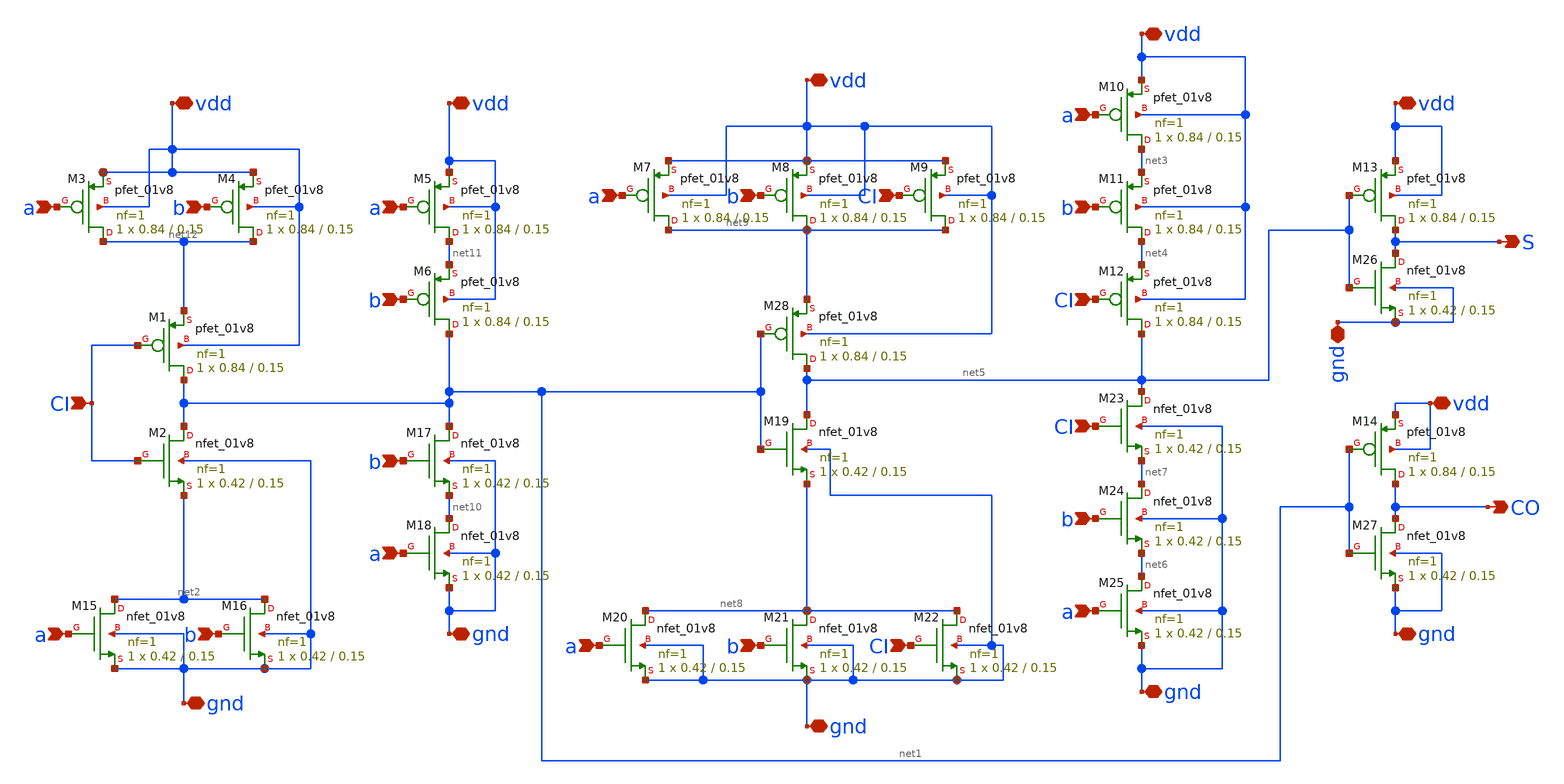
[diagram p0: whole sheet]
** sch_path: Adder/xschem/addf.sch
**.subckt addf CI CO S a a a a a a a a b b b b b b b b CI CI CI CI vdd gnd vdd vdd vdd vdd vdd gnd
*+ gnd gnd gnd gnd
*.ipin CI
*.opin CO
*.opin S
*.ipin a
*.ipin a
*.ipin a
*.ipin a
*.ipin a
*.ipin a
*.ipin a
*.ipin a
*.ipin b
*.ipin b
*.ipin b
*.ipin b
*.ipin b
*.ipin b
*.ipin b
*.ipin b
*.ipin CI
*.ipin CI
*.ipin CI
*.ipin CI
*.iopin vdd
*.iopin gnd
*.iopin vdd
*.iopin vdd
*.iopin vdd
*.iopin vdd
*.iopin vdd
*.iopin gnd
*.iopin gnd
*.iopin gnd
*.iopin gnd
*.iopin gnd
XM1 net1 CI net12 vdd sky130_fd_pr__pfet_01v8 L=0.15 W=0.84 nf=1 ad='int((nf+1)/2) * W/nf * 0.29' as='int((nf+2)/2) * W/nf * 0.29'
+ pd='2*int((nf+1)/2) * (W/nf + 0.29)' ps='2*int((nf+2)/2) * (W/nf + 0.29)' nrd='0.29 / W' nrs='0.29 / W'
+ sa=0 sb=0 sd=0 mult=1 m=1
XM2 net1 CI net2 gnd sky130_fd_pr__nfet_01v8 L=0.15 W=0.42 nf=1 ad='int((nf+1)/2) * W/nf * 0.29' as='int((nf+2)/2) * W/nf * 0.29'
+ pd='2*int((nf+1)/2) * (W/nf + 0.29)' ps='2*int((nf+2)/2) * (W/nf + 0.29)' nrd='0.29 / W' nrs='0.29 / W'
+ sa=0 sb=0 sd=0 mult=1 m=1
XM3 net12 a vdd vdd sky130_fd_pr__pfet_01v8 L=0.15 W=0.84 nf=1 ad='int((nf+1)/2) * W/nf * 0.29' as='int((nf+2)/2) * W/nf * 0.29'
+ pd='2*int((nf+1)/2) * (W/nf + 0.29)' ps='2*int((nf+2)/2) * (W/nf + 0.29)' nrd='0.29 / W' nrs='0.29 / W'
+ sa=0 sb=0 sd=0 mult=1 m=1
XM4 net12 b vdd vdd sky130_fd_pr__pfet_01v8 L=0.15 W=0.84 nf=1 ad='int((nf+1)/2) * W/nf * 0.29' as='int((nf+2)/2) * W/nf * 0.29'
+ pd='2*int((nf+1)/2) * (W/nf + 0.29)' ps='2*int((nf+2)/2) * (W/nf + 0.29)' nrd='0.29 / W' nrs='0.29 / W'
+ sa=0 sb=0 sd=0 mult=1 m=1
XM5 net11 a vdd vdd sky130_fd_pr__pfet_01v8 L=0.15 W=0.84 nf=1 ad='int((nf+1)/2) * W/nf * 0.29' as='int((nf+2)/2) * W/nf * 0.29'
+ pd='2*int((nf+1)/2) * (W/nf + 0.29)' ps='2*int((nf+2)/2) * (W/nf + 0.29)' nrd='0.29 / W' nrs='0.29 / W'
+ sa=0 sb=0 sd=0 mult=1 m=1
XM6 net1 b net11 vdd sky130_fd_pr__pfet_01v8 L=0.15 W=0.84 nf=1 ad='int((nf+1)/2) * W/nf * 0.29' as='int((nf+2)/2) * W/nf * 0.29'
+ pd='2*int((nf+1)/2) * (W/nf + 0.29)' ps='2*int((nf+2)/2) * (W/nf + 0.29)' nrd='0.29 / W' nrs='0.29 / W'
+ sa=0 sb=0 sd=0 mult=1 m=1
XM7 net9 a vdd vdd sky130_fd_pr__pfet_01v8 L=0.15 W=0.84 nf=1 ad='int((nf+1)/2) * W/nf * 0.29' as='int((nf+2)/2) * W/nf * 0.29'
+ pd='2*int((nf+1)/2) * (W/nf + 0.29)' ps='2*int((nf+2)/2) * (W/nf + 0.29)' nrd='0.29 / W' nrs='0.29 / W'
+ sa=0 sb=0 sd=0 mult=1 m=1
XM8 net9 b vdd vdd sky130_fd_pr__pfet_01v8 L=0.15 W=0.84 nf=1 ad='int((nf+1)/2) * W/nf * 0.29' as='int((nf+2)/2) * W/nf * 0.29'
+ pd='2*int((nf+1)/2) * (W/nf + 0.29)' ps='2*int((nf+2)/2) * (W/nf + 0.29)' nrd='0.29 / W' nrs='0.29 / W'
+ sa=0 sb=0 sd=0 mult=1 m=1
XM9 net9 CI vdd vdd sky130_fd_pr__pfet_01v8 L=0.15 W=0.84 nf=1 ad='int((nf+1)/2) * W/nf * 0.29' as='int((nf+2)/2) * W/nf * 0.29'
+ pd='2*int((nf+1)/2) * (W/nf + 0.29)' ps='2*int((nf+2)/2) * (W/nf + 0.29)' nrd='0.29 / W' nrs='0.29 / W'
+ sa=0 sb=0 sd=0 mult=1 m=1
XM10 net3 a vdd vdd sky130_fd_pr__pfet_01v8 L=0.15 W=0.84 nf=1 ad='int((nf+1)/2) * W/nf * 0.29' as='int((nf+2)/2) * W/nf * 0.29'
+ pd='2*int((nf+1)/2) * (W/nf + 0.29)' ps='2*int((nf+2)/2) * (W/nf + 0.29)' nrd='0.29 / W' nrs='0.29 / W'
+ sa=0 sb=0 sd=0 mult=1 m=1
XM11 net4 b net3 vdd sky130_fd_pr__pfet_01v8 L=0.15 W=0.84 nf=1 ad='int((nf+1)/2) * W/nf * 0.29' as='int((nf+2)/2) * W/nf * 0.29'
+ pd='2*int((nf+1)/2) * (W/nf + 0.29)' ps='2*int((nf+2)/2) * (W/nf + 0.29)' nrd='0.29 / W' nrs='0.29 / W'
+ sa=0 sb=0 sd=0 mult=1 m=1
XM12 net5 CI net4 vdd sky130_fd_pr__pfet_01v8 L=0.15 W=0.84 nf=1 ad='int((nf+1)/2) * W/nf * 0.29' as='int((nf+2)/2) * W/nf * 0.29'
+ pd='2*int((nf+1)/2) * (W/nf + 0.29)' ps='2*int((nf+2)/2) * (W/nf + 0.29)' nrd='0.29 / W' nrs='0.29 / W'
+ sa=0 sb=0 sd=0 mult=1 m=1
XM13 S net5 vdd vdd sky130_fd_pr__pfet_01v8 L=0.15 W=0.84 nf=1 ad='int((nf+1)/2) * W/nf * 0.29' as='int((nf+2)/2) * W/nf * 0.29'
+ pd='2*int((nf+1)/2) * (W/nf + 0.29)' ps='2*int((nf+2)/2) * (W/nf + 0.29)' nrd='0.29 / W' nrs='0.29 / W'
+ sa=0 sb=0 sd=0 mult=1 m=1
XM14 CO net1 vdd vdd sky130_fd_pr__pfet_01v8 L=0.15 W=0.84 nf=1 ad='int((nf+1)/2) * W/nf * 0.29' as='int((nf+2)/2) * W/nf * 0.29'
+ pd='2*int((nf+1)/2) * (W/nf + 0.29)' ps='2*int((nf+2)/2) * (W/nf + 0.29)' nrd='0.29 / W' nrs='0.29 / W'
+ sa=0 sb=0 sd=0 mult=1 m=1
XM15 net2 a gnd gnd sky130_fd_pr__nfet_01v8 L=0.15 W=0.42 nf=1 ad='int((nf+1)/2) * W/nf * 0.29' as='int((nf+2)/2) * W/nf * 0.29'
+ pd='2*int((nf+1)/2) * (W/nf + 0.29)' ps='2*int((nf+2)/2) * (W/nf + 0.29)' nrd='0.29 / W' nrs='0.29 / W'
+ sa=0 sb=0 sd=0 mult=1 m=1
XM16 net2 b gnd gnd sky130_fd_pr__nfet_01v8 L=0.15 W=0.42 nf=1 ad='int((nf+1)/2) * W/nf * 0.29' as='int((nf+2)/2) * W/nf * 0.29'
+ pd='2*int((nf+1)/2) * (W/nf + 0.29)' ps='2*int((nf+2)/2) * (W/nf + 0.29)' nrd='0.29 / W' nrs='0.29 / W'
+ sa=0 sb=0 sd=0 mult=1 m=1
XM17 net1 b net10 gnd sky130_fd_pr__nfet_01v8 L=0.15 W=0.42 nf=1 ad='int((nf+1)/2) * W/nf * 0.29' as='int((nf+2)/2) * W/nf * 0.29'
+ pd='2*int((nf+1)/2) * (W/nf + 0.29)' ps='2*int((nf+2)/2) * (W/nf + 0.29)' nrd='0.29 / W' nrs='0.29 / W'
+ sa=0 sb=0 sd=0 mult=1 m=1
XM18 net10 a gnd gnd sky130_fd_pr__nfet_01v8 L=0.15 W=0.42 nf=1 ad='int((nf+1)/2) * W/nf * 0.29' as='int((nf+2)/2) * W/nf * 0.29'
+ pd='2*int((nf+1)/2) * (W/nf + 0.29)' ps='2*int((nf+2)/2) * (W/nf + 0.29)' nrd='0.29 / W' nrs='0.29 / W'
+ sa=0 sb=0 sd=0 mult=1 m=1
XM19 net5 net1 net8 gnd sky130_fd_pr__nfet_01v8 L=0.15 W=0.42 nf=1 ad='int((nf+1)/2) * W/nf * 0.29' as='int((nf+2)/2) * W/nf * 0.29'
+ pd='2*int((nf+1)/2) * (W/nf + 0.29)' ps='2*int((nf+2)/2) * (W/nf + 0.29)' nrd='0.29 / W' nrs='0.29 / W'
+ sa=0 sb=0 sd=0 mult=1 m=1
XM20 net8 a gnd gnd sky130_fd_pr__nfet_01v8 L=0.15 W=0.42 nf=1 ad='int((nf+1)/2) * W/nf * 0.29' as='int((nf+2)/2) * W/nf * 0.29'
+ pd='2*int((nf+1)/2) * (W/nf + 0.29)' ps='2*int((nf+2)/2) * (W/nf + 0.29)' nrd='0.29 / W' nrs='0.29 / W'
+ sa=0 sb=0 sd=0 mult=1 m=1
XM21 net8 b gnd gnd sky130_fd_pr__nfet_01v8 L=0.15 W=0.42 nf=1 ad='int((nf+1)/2) * W/nf * 0.29' as='int((nf+2)/2) * W/nf * 0.29'
+ pd='2*int((nf+1)/2) * (W/nf + 0.29)' ps='2*int((nf+2)/2) * (W/nf + 0.29)' nrd='0.29 / W' nrs='0.29 / W'
+ sa=0 sb=0 sd=0 mult=1 m=1
XM22 net8 CI gnd gnd sky130_fd_pr__nfet_01v8 L=0.15 W=0.42 nf=1 ad='int((nf+1)/2) * W/nf * 0.29' as='int((nf+2)/2) * W/nf * 0.29'
+ pd='2*int((nf+1)/2) * (W/nf + 0.29)' ps='2*int((nf+2)/2) * (W/nf + 0.29)' nrd='0.29 / W' nrs='0.29 / W'
+ sa=0 sb=0 sd=0 mult=1 m=1
XM23 net5 CI net7 gnd sky130_fd_pr__nfet_01v8 L=0.15 W=0.42 nf=1 ad='int((nf+1)/2) * W/nf * 0.29' as='int((nf+2)/2) * W/nf * 0.29'
+ pd='2*int((nf+1)/2) * (W/nf + 0.29)' ps='2*int((nf+2)/2) * (W/nf + 0.29)' nrd='0.29 / W' nrs='0.29 / W'
+ sa=0 sb=0 sd=0 mult=1 m=1
XM24 net7 b net6 gnd sky130_fd_pr__nfet_01v8 L=0.15 W=0.42 nf=1 ad='int((nf+1)/2) * W/nf * 0.29' as='int((nf+2)/2) * W/nf * 0.29'
+ pd='2*int((nf+1)/2) * (W/nf + 0.29)' ps='2*int((nf+2)/2) * (W/nf + 0.29)' nrd='0.29 / W' nrs='0.29 / W'
+ sa=0 sb=0 sd=0 mult=1 m=1
XM25 net6 a gnd gnd sky130_fd_pr__nfet_01v8 L=0.15 W=0.42 nf=1 ad='int((nf+1)/2) * W/nf * 0.29' as='int((nf+2)/2) * W/nf * 0.29'
+ pd='2*int((nf+1)/2) * (W/nf + 0.29)' ps='2*int((nf+2)/2) * (W/nf + 0.29)' nrd='0.29 / W' nrs='0.29 / W'
+ sa=0 sb=0 sd=0 mult=1 m=1
XM26 S net5 gnd gnd sky130_fd_pr__nfet_01v8 L=0.15 W=0.42 nf=1 ad='int((nf+1)/2) * W/nf * 0.29' as='int((nf+2)/2) * W/nf * 0.29'
+ pd='2*int((nf+1)/2) * (W/nf + 0.29)' ps='2*int((nf+2)/2) * (W/nf + 0.29)' nrd='0.29 / W' nrs='0.29 / W'
+ sa=0 sb=0 sd=0 mult=1 m=1
XM27 CO net1 gnd gnd sky130_fd_pr__nfet_01v8 L=0.15 W=0.42 nf=1 ad='int((nf+1)/2) * W/nf * 0.29' as='int((nf+2)/2) * W/nf * 0.29'
+ pd='2*int((nf+1)/2) * (W/nf + 0.29)' ps='2*int((nf+2)/2) * (W/nf + 0.29)' nrd='0.29 / W' nrs='0.29 / W'
+ sa=0 sb=0 sd=0 mult=1 m=1
XM28 net5 net1 net9 vdd sky130_fd_pr__pfet_01v8 L=0.15 W=0.84 nf=1 ad='int((nf+1)/2) * W/nf * 0.29' as='int((nf+2)/2) * W/nf * 0.29'
+ pd='2*int((nf+1)/2) * (W/nf + 0.29)' ps='2*int((nf+2)/2) * (W/nf + 0.29)' nrd='0.29 / W' nrs='0.29 / W'
+ sa=0 sb=0 sd=0 mult=1 m=1
**.ends
.end
